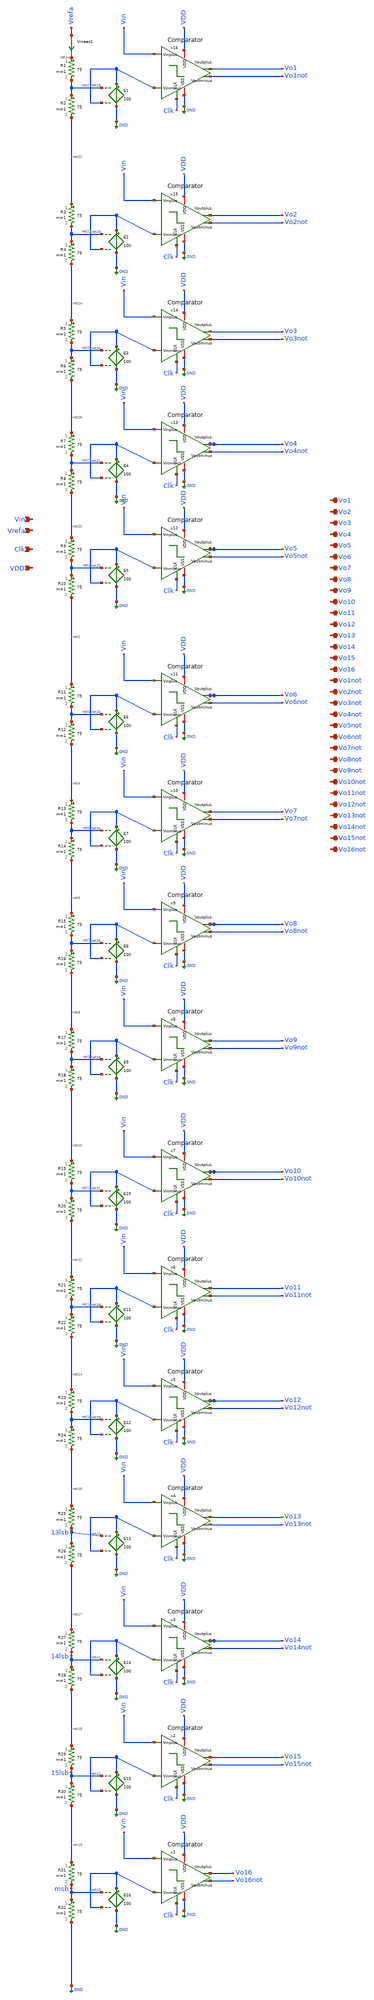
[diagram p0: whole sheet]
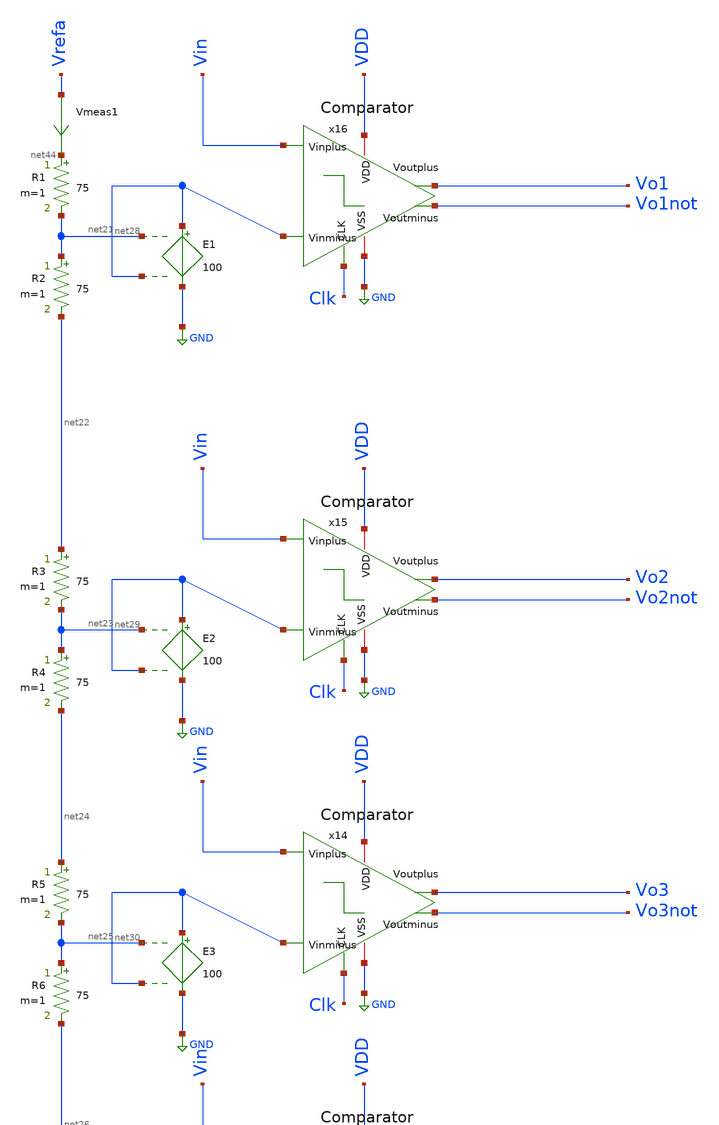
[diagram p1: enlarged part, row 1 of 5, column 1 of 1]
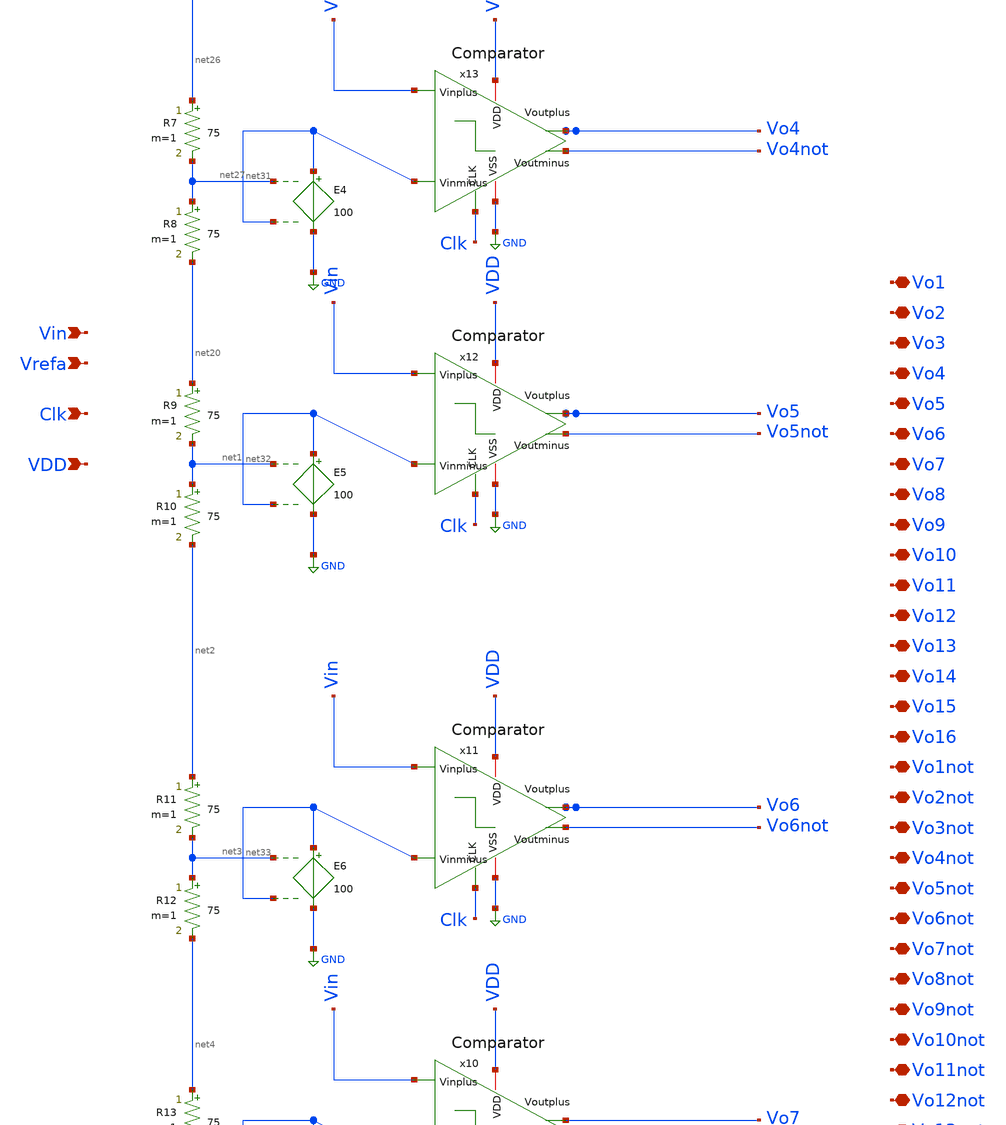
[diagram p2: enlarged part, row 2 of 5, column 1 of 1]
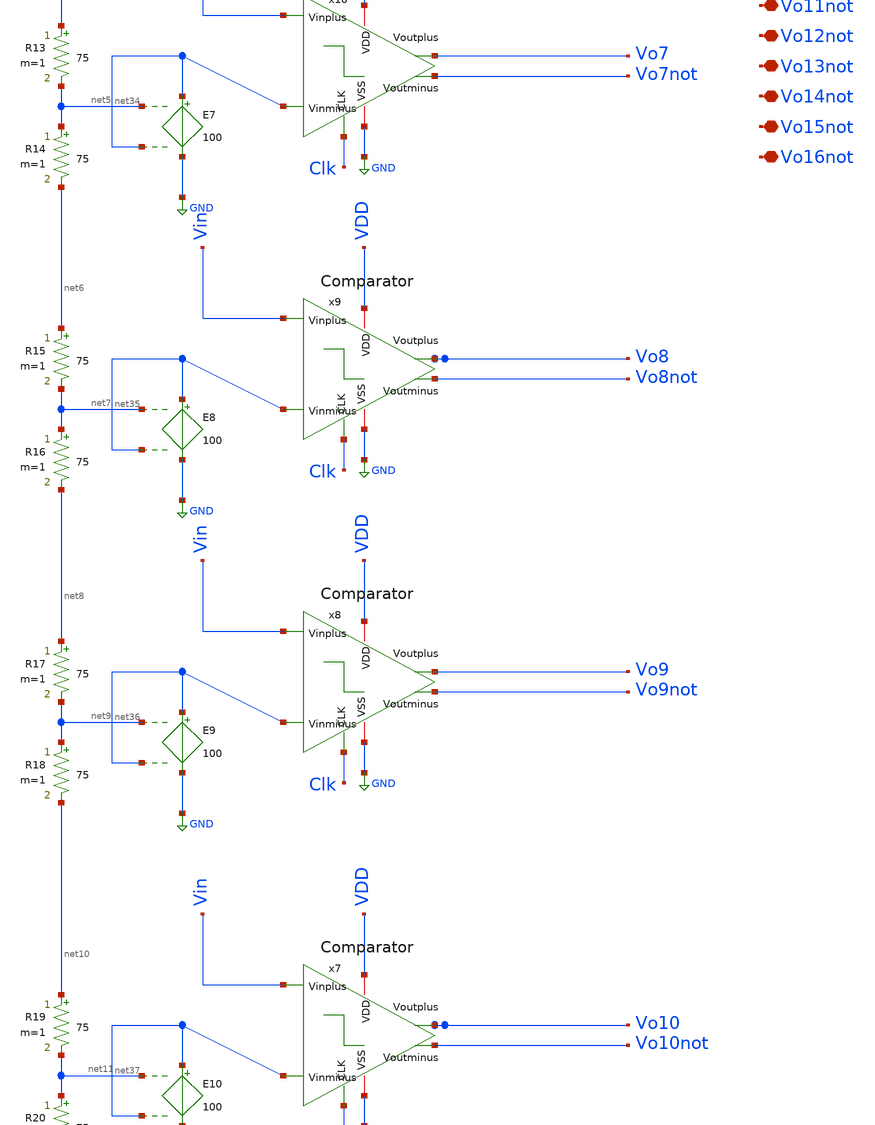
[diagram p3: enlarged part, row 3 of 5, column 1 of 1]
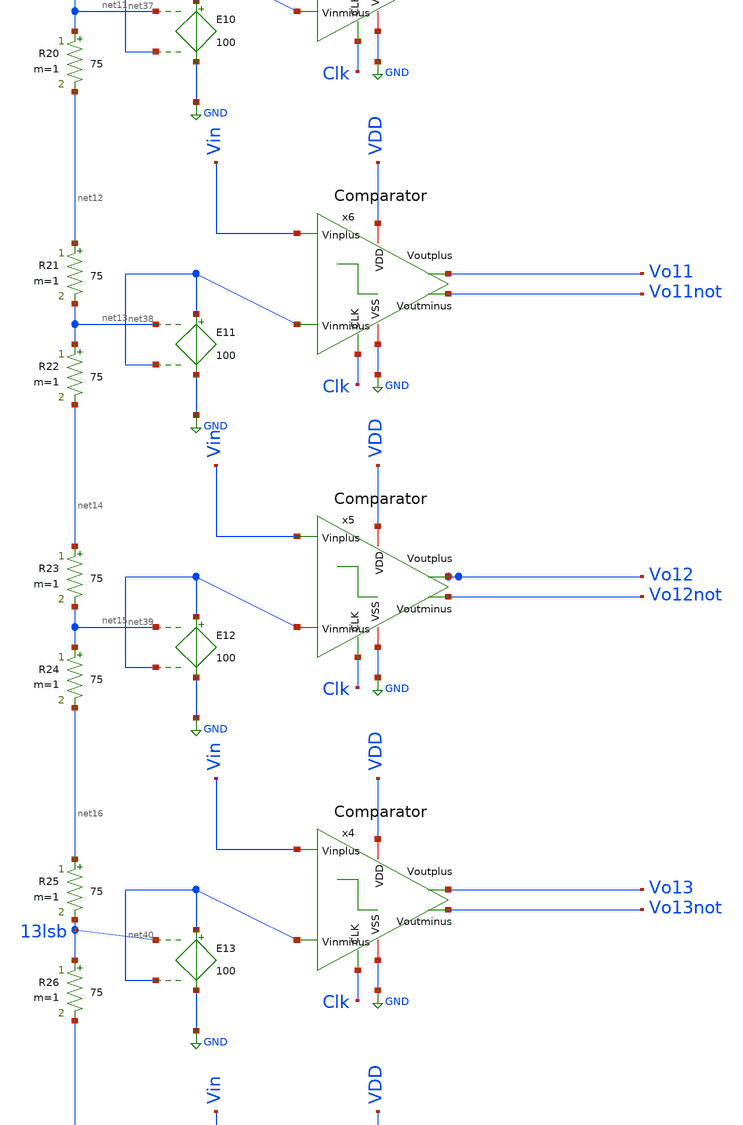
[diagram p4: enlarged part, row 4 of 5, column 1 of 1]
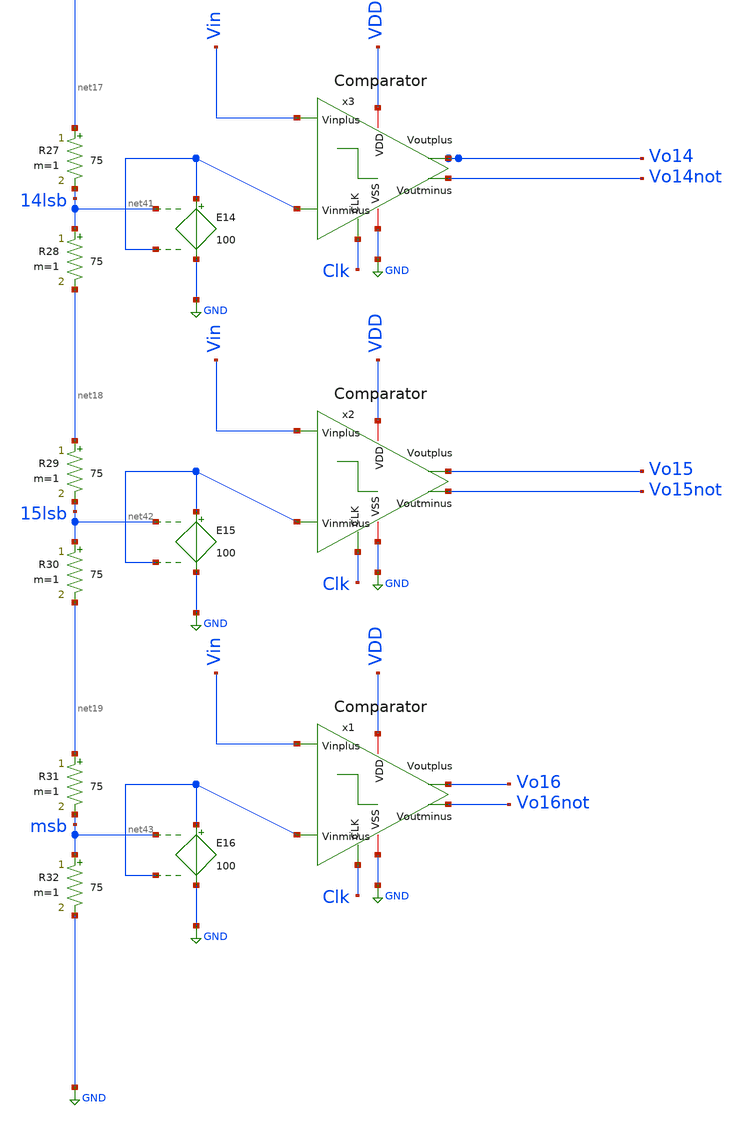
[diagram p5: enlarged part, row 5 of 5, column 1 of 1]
** sch_path: xschem/DataConverters/4bitADC2.sch
**.subckt 4bitADC2 Vin Vrefa Clk VDD Vo1 Vo2 Vo3 Vo4 Vo5 Vo6 Vo7 Vo8 Vo9 Vo10 Vo11 Vo12 Vo13 Vo14
*+ Vo16 Vo16not Vo14not Vo13not Vo12not Vo11not Vo10not Vo9not Vo8not Vo7not Vo6not Vo5not Vo4not Vo3not
*+ Vo2not Vo1not Vo15 Vo15not
*.ipin Vin
*.ipin Vrefa
*.ipin Clk
*.ipin VDD
*.iopin Vo1
*.iopin Vo2
*.iopin Vo3
*.iopin Vo4
*.iopin Vo5
*.iopin Vo6
*.iopin Vo7
*.iopin Vo8
*.iopin Vo9
*.iopin Vo10
*.iopin Vo11
*.iopin Vo12
*.iopin Vo13
*.iopin Vo14
*.iopin Vo16
*.iopin Vo16not
*.iopin Vo14not
*.iopin Vo13not
*.iopin Vo12not
*.iopin Vo11not
*.iopin Vo10not
*.iopin Vo9not
*.iopin Vo8not
*.iopin Vo7not
*.iopin Vo6not
*.iopin Vo5not
*.iopin Vo4not
*.iopin Vo3not
*.iopin Vo2not
*.iopin Vo1not
*.iopin Vo15
*.iopin Vo15not
Vmeas1 Vrefa net44 0
.save i(vmeas1)
R1 net44 net21 75 m=1
R2 net21 net22 75 m=1
R3 net22 net23 75 m=1
R4 net23 net24 75 m=1
R5 net24 net25 75 m=1
R6 net25 net26 75 m=1
R7 net26 net27 75 m=1
R8 net27 net20 75 m=1
R9 net20 net1 75 m=1
R10 net1 net2 75 m=1
R11 net2 net3 75 m=1
R12 net3 net4 75 m=1
R13 net4 net5 75 m=1
R14 net5 net6 75 m=1
R15 net6 net7 75 m=1
R16 net7 net8 75 m=1
R17 net8 net9 75 m=1
R18 net9 net10 75 m=1
R19 net10 net11 75 m=1
R20 net11 net12 75 m=1
R21 net12 net13 75 m=1
R22 net13 net14 75 m=1
R23 net14 net15 75 m=1
R24 net15 net16 75 m=1
R25 net16 13lsb 75 m=1
R26 13lsb net17 75 m=1
R27 net17 14lsb 75 m=1
R28 14lsb net18 75 m=1
R29 net18 15lsb 75 m=1
R30 15lsb net19 75 m=1
R31 net19 msb 75 m=1
R32 msb GND 75 m=1
x1 VDD Vo16not Vo16 Clk Vin net43 GND Comparator
x2 VDD Vo15not Vo15 Clk Vin net42 GND Comparator
x3 VDD Vo14not Vo14 Clk Vin net41 GND Comparator
x4 VDD Vo13not Vo13 Clk Vin net40 GND Comparator
x5 VDD Vo12not Vo12 Clk Vin net39 GND Comparator
x6 VDD Vo11not Vo11 Clk Vin net38 GND Comparator
x7 VDD Vo10not Vo10 Clk Vin net37 GND Comparator
x8 VDD Vo9not Vo9 Clk Vin net36 GND Comparator
x9 VDD Vo8not Vo8 Clk Vin net35 GND Comparator
x10 VDD Vo7not Vo7 Clk Vin net34 GND Comparator
x11 VDD Vo6not Vo6 Clk Vin net33 GND Comparator
x12 VDD Vo5not Vo5 Clk Vin net32 GND Comparator
x13 VDD Vo4not Vo4 Clk Vin net31 GND Comparator
x14 VDD Vo3not Vo3 Clk Vin net30 GND Comparator
x15 VDD Vo2not Vo2 Clk Vin net29 GND Comparator
x16 VDD Vo1not Vo1 Clk Vin net28 GND Comparator
E1 net28 GND net21 net28 100
E2 net29 GND net23 net29 100
E3 net30 GND net25 net30 100
E4 net31 GND net27 net31 100
E5 net32 GND net1 net32 100
E6 net33 GND net3 net33 100
E7 net34 GND net5 net34 100
E8 net35 GND net7 net35 100
E9 net36 GND net9 net36 100
E10 net37 GND net11 net37 100
E11 net38 GND net13 net38 100
E12 net39 GND net15 net39 100
E13 net40 GND 13lsb net40 100
E14 net41 GND 14lsb net41 100
E15 net42 GND 15lsb net42 100
E16 net43 GND msb net43 100
**.ends
.GLOBAL GND
.end
